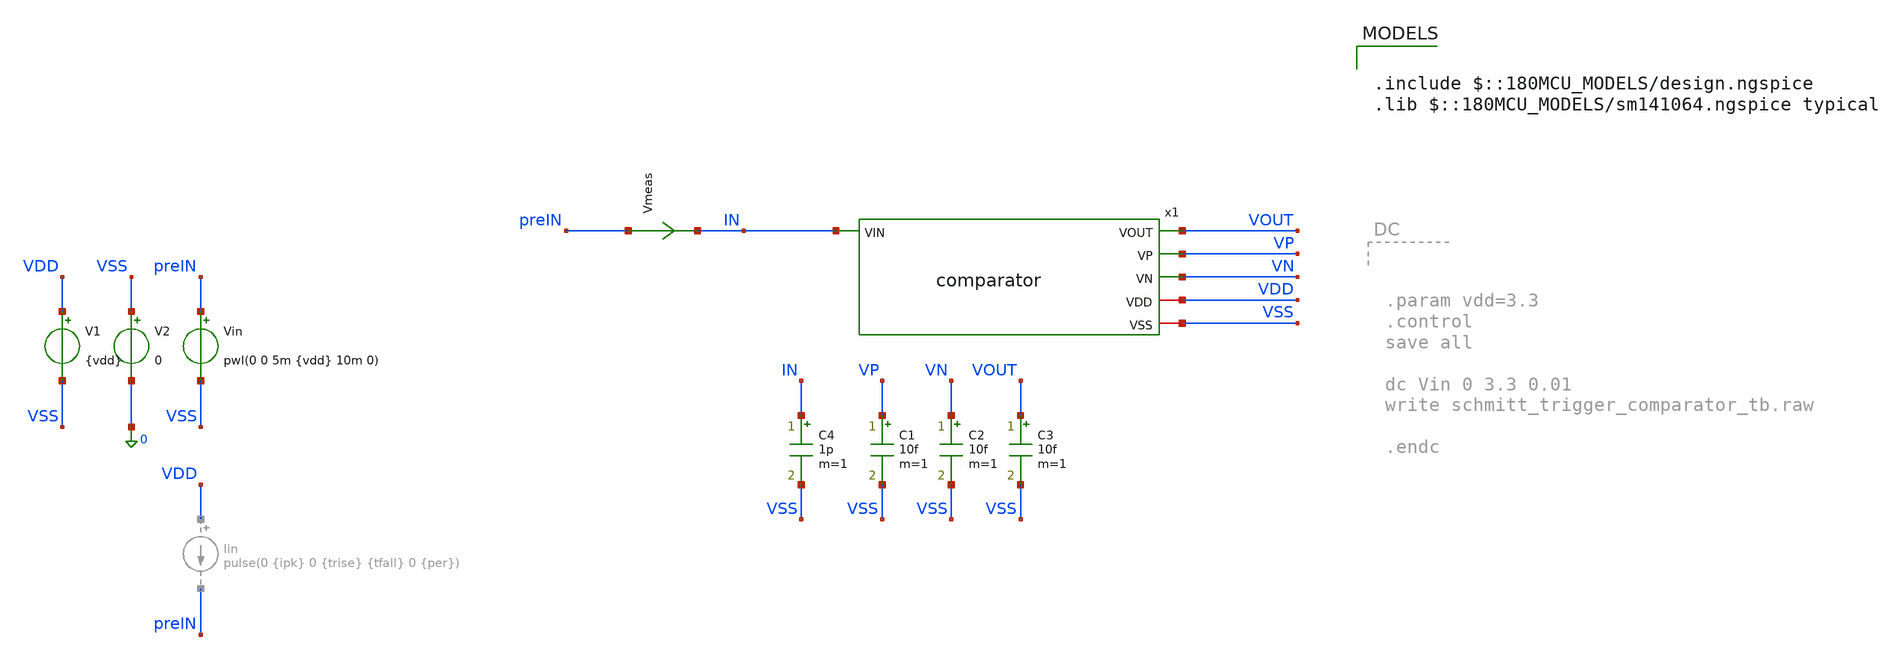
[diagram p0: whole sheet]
** sch_path: analog/neuron/schmitt_trigger_comparator_testbench.sch
**.subckt schmitt_trigger_comparator_testbench
V1 VDD VSS {vdd}
V2 VSS 0 0
Vin preIN VSS pwl(0 0 5m {vdd} 10m 0)
C1 VP VSS 10f m=1
C2 VN VSS 10f m=1
C3 VOUT VSS 10f m=1
C4 IN VSS 1p m=1
Vmeas preIN IN 0
.save i(vmeas)
x1 IN VOUT VP VN VDD VSS comparator
**** begin user architecture code

.include $::180MCU_MODELS/design.ngspice
.lib $::180MCU_MODELS/sm141064.ngspice typical



.param vdd=3.3
.control
	save all
	tran 1u 10m
	meas tran vthp FIND v(in) WHEN v(vout)=1.65 FALL=1
	meas tran vthn FIND v(in) WHEN v(vout)=1.65 RISE=1
	let vhys=vthp-vthn
	echo 'VTH+ = $&vthp VTH- = $&vthn hysteresis = $&vhys'
	wrdata /foss/designs/engn2912e-project/analog/neuron/comparator_tb.txt v(in) v(vout)
	plot v(vout) vs v(in)
	plot v(vout) v(in)
.endc


**** end user architecture code
**.ends
.end
